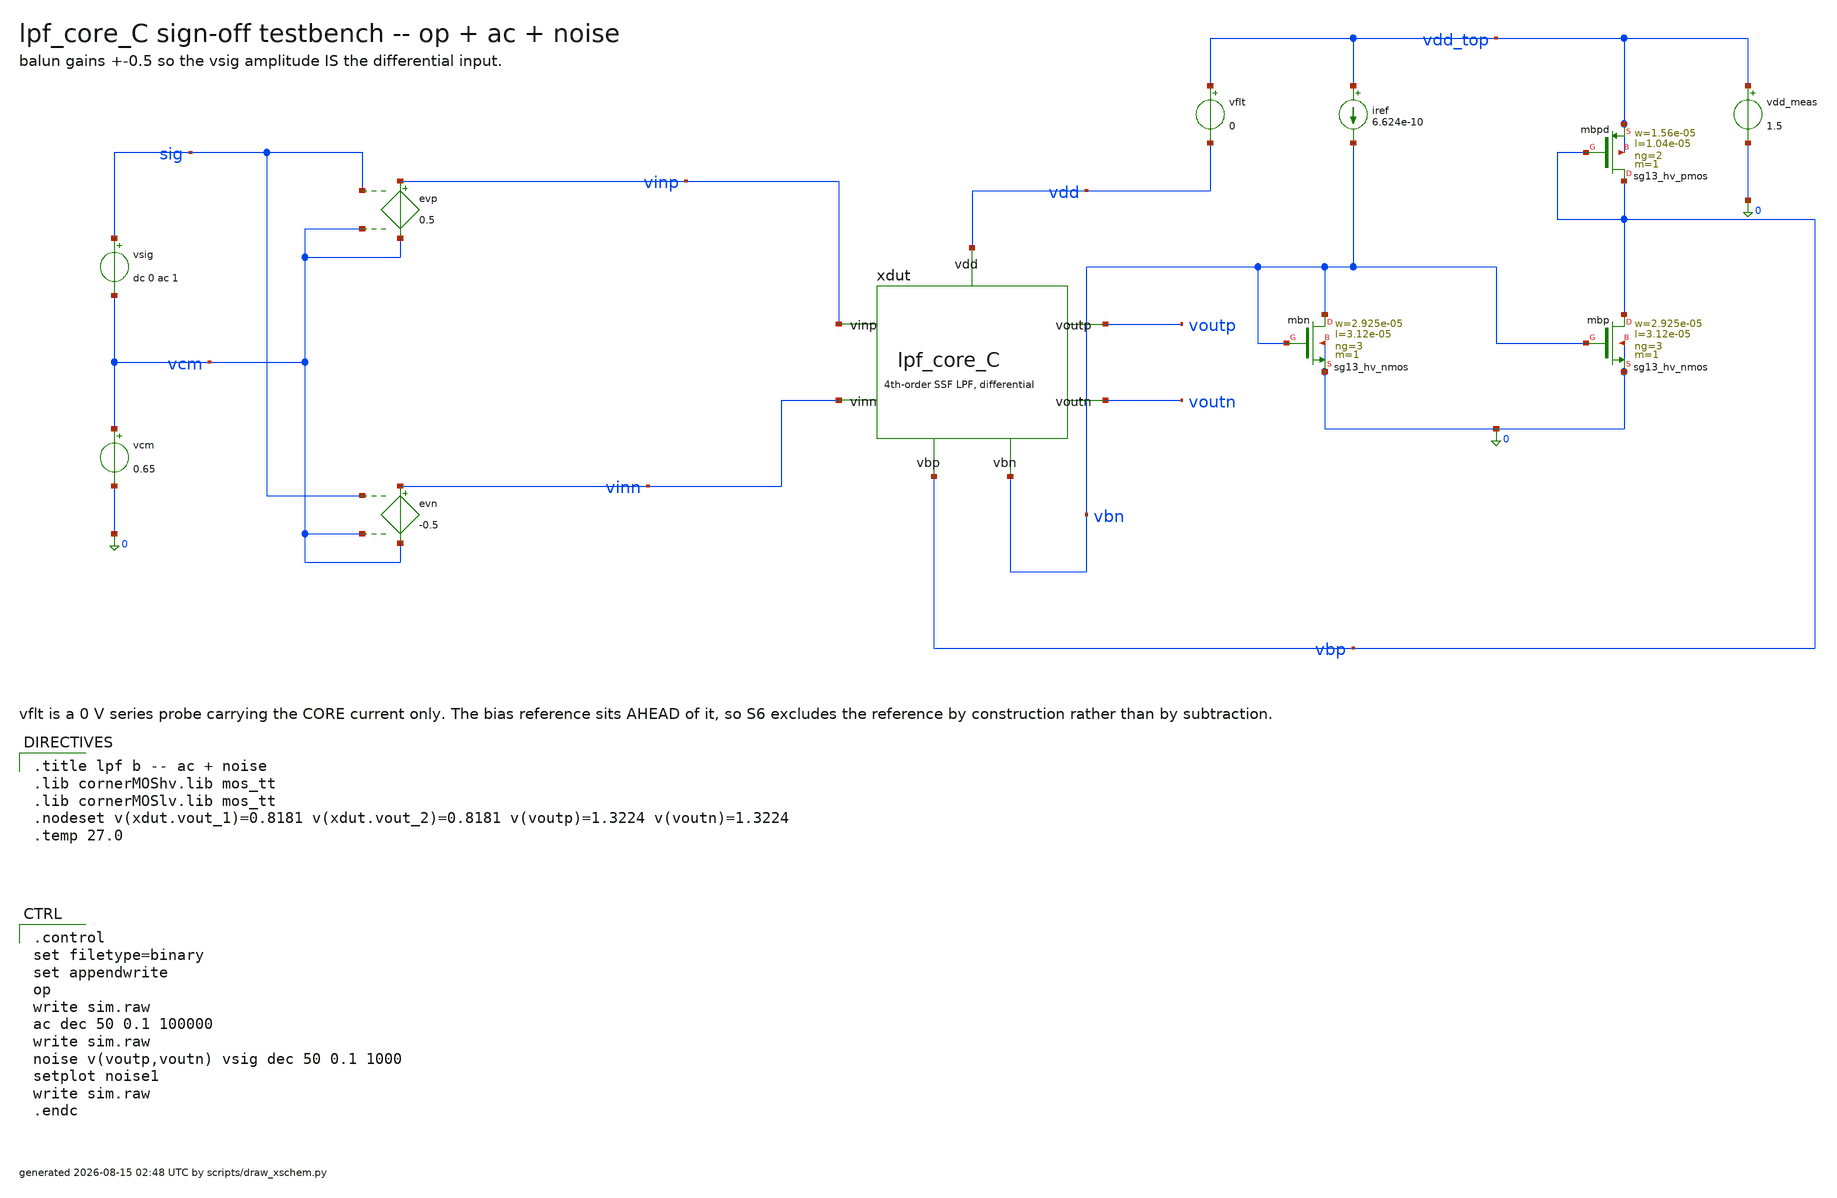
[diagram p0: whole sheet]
** sch_path: signoff/pre-pvt/C-lownoise/lpf_tb_C.sch
**.subckt lpf_tb_C
vsig sig vcm dc 0 ac 1
vcm vcm 0 0.65
evp vinp vcm sig vcm 0.5
evn vinn vcm sig vcm -0.5
xdut vinp vinn voutp voutn vbn vbp vdd lpf_core_C
vflt vdd_top vdd 0
vdd_meas vdd_top 0 1.5
iref vdd_top vbn 6.624e-10
Xmbn vbn vbn 0 0 sg13_hv_nmos w=2.925e-05 l=3.12e-05 ng=3 m=1 mm_ok=1
Xmbp vbp vbn 0 0 sg13_hv_nmos w=2.925e-05 l=3.12e-05 ng=3 m=1 mm_ok=1
Xmbpd vbp vbp vdd_top vdd_top sg13_hv_pmos w=1.56e-05 l=1.04e-05 ng=2 m=1 mm_ok=1
**** begin user architecture code

.title lpf b -- ac + noise
.lib cornerMOShv.lib mos_tt
.lib cornerMOSlv.lib mos_tt
.nodeset v(xdut.vout_1)=0.8181 v(xdut.vout_2)=0.8181 v(voutp)=1.3224 v(voutn)=1.3224
.temp 27.0


.control
set filetype=binary
set appendwrite
op
write sim.raw
ac dec 50 0.1 100000
write sim.raw
noise v(voutp,voutn) vsig dec 50 0.1 1000
setplot noise1
write sim.raw
.endc

**** end user architecture code
**.ends
.end
